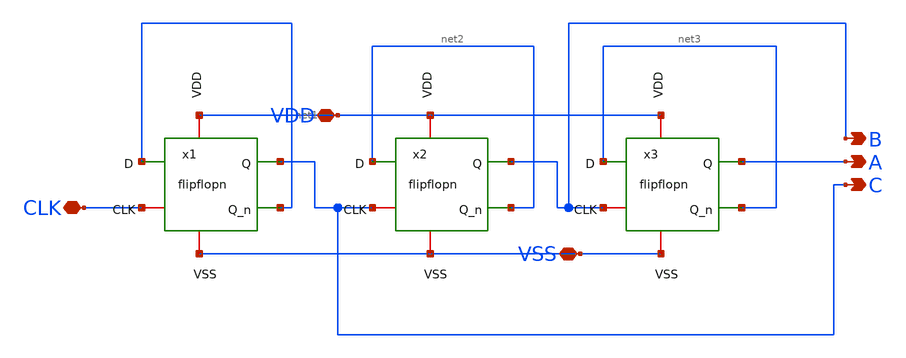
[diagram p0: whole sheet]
** sch_path: xschem/cont3.sch
**.subckt cont3 B CLK VDD VSS A C
*.opin B
*.iopin CLK
*.iopin VDD
*.iopin VSS
*.opin A
*.opin C
x1 CLK net1 VDD C net1 VSS flipflopn
x2 C net2 VDD B net2 VSS flipflopn
x3 B net3 VDD A net3 VSS flipflopn
**.ends
.end
